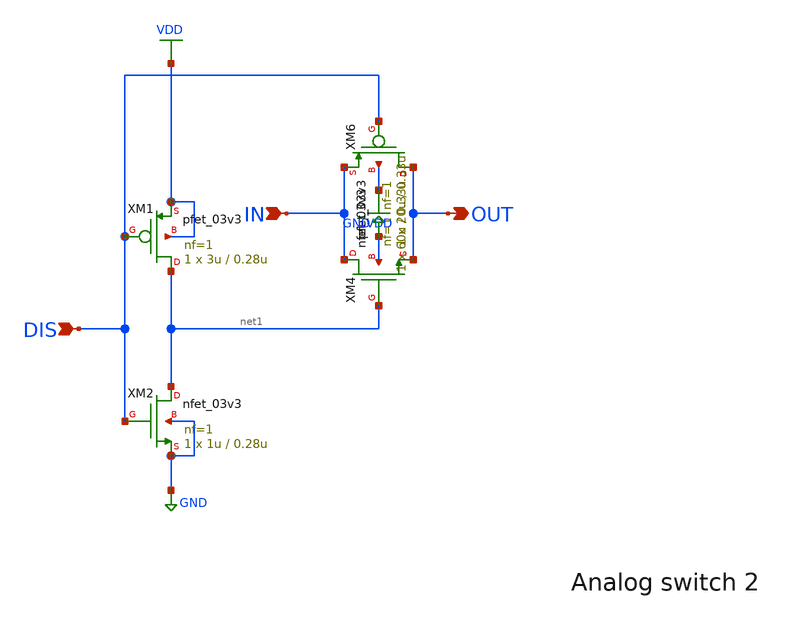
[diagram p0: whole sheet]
** sch_path: pex_io/sw.sch
**.subckt sw OUT IN DIS
*.opin OUT
*.ipin IN
*.ipin DIS
XM1 net1 DIS VDD VDD pfet_03v3 L=0.28u W=3u nf=1 ad='int((nf+1)/2) * W/nf * 0.18u' as='int((nf+2)/2) * W/nf * 0.18u'
+ pd='2*int((nf+1)/2) * (W/nf + 0.18u)' ps='2*int((nf+2)/2) * (W/nf + 0.18u)' nrd='0.18u / W' nrs='0.18u / W'
+ sa=0 sb=0 sd=0 m=1
XM2 net1 DIS GND GND nfet_03v3 L=0.28u W=1u nf=1 ad='int((nf+1)/2) * W/nf * 0.18u' as='int((nf+2)/2) * W/nf * 0.18u'
+ pd='2*int((nf+1)/2) * (W/nf + 0.18u)' ps='2*int((nf+2)/2) * (W/nf + 0.18u)' nrd='0.18u / W' nrs='0.18u / W'
+ sa=0 sb=0 sd=0 m=1
XM4 IN net1 OUT GND nfet_03v3 L=0.33u W=20u nf=1 ad='int((nf+1)/2) * W/nf * 0.18u' as='int((nf+2)/2) * W/nf * 0.18u'
+ pd='2*int((nf+1)/2) * (W/nf + 0.18u)' ps='2*int((nf+2)/2) * (W/nf + 0.18u)' nrd='0.18u / W' nrs='0.18u / W'
+ sa=0 sb=0 sd=0 m=1
XM6 OUT DIS IN VDD pfet_03v3 L=0.33u W=60u nf=1 ad='int((nf+1)/2) * W/nf * 0.18u' as='int((nf+2)/2) * W/nf * 0.18u'
+ pd='2*int((nf+1)/2) * (W/nf + 0.18u)' ps='2*int((nf+2)/2) * (W/nf + 0.18u)' nrd='0.18u / W' nrs='0.18u / W'
+ sa=0 sb=0 sd=0 m=1
**.ends
.GLOBAL VDD
.GLOBAL GND
.end
